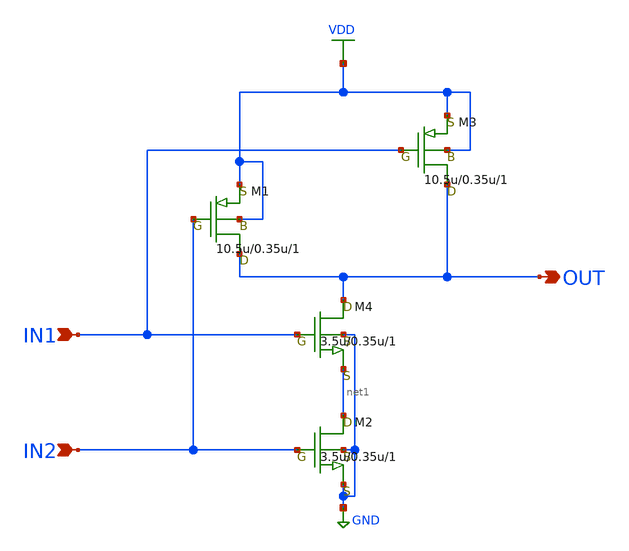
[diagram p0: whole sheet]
** sch_path: LR_hokari/LR_Work2/NAND2.sch
**.subckt NAND2 IN1 IN2 OUT
*.ipin IN1
*.ipin IN2
*.opin OUT
M1 OUT IN2 VDD VDD pch w=10.5u l=0.35u as=0 ps=0 ad=0 pd=0 m=1
M2 net1 IN2 GND GND nch w=3.5u l=0.35u as=0 ps=0 ad=0 pd=0 m=1
M3 OUT IN1 VDD VDD pch w=10.5u l=0.35u as=0 ps=0 ad=0 pd=0 m=1
M4 OUT IN1 net1 GND nch w=3.5u l=0.35u as=0 ps=0 ad=0 pd=0 m=1
**.ends
.GLOBAL VDD
.GLOBAL GND
.end
